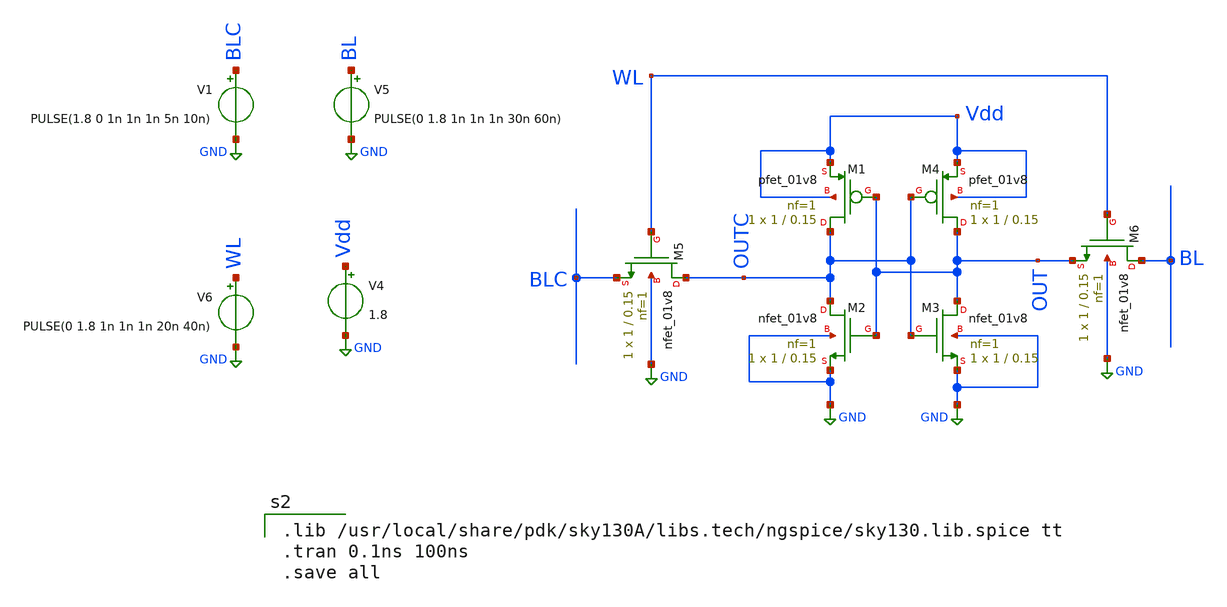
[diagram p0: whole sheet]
** sch_path: Schematic/SRam/SRam.sch
**.subckt SRam
XM2 OUTC OUT GND GND sky130_fd_pr__nfet_01v8 L=0.15 W=1 nf=1 ad='int((1 + 1)/2) * 1 / 1 * 0.29' as='int((1 + 2)/2) * 1 / 1 * 0.29'
+ pd='2*int((1 + 1)/2) * (1 / 1 + 0.29)' ps='2*int((1 + 2)/2) * (1 / 1 + 0.29)' nrd='0.29 / 1 ' nrs='0.29 / 1 '
+ sa=0 sb=0 sd=0 mult=1 m=1
XM1 OUTC OUT Vdd Vdd sky130_fd_pr__pfet_01v8 L=0.15 W=1 nf=1 ad='int((1 + 1)/2) * 1 / 1 * 0.29' as='int((1 + 2)/2) * 1 / 1 * 0.29'
+ pd='2*int((1 + 1)/2) * (1 / 1 + 0.29)' ps='2*int((1 + 2)/2) * (1 / 1 + 0.29)' nrd='0.29 / 1 ' nrs='0.29 / 1 '
+ sa=0 sb=0 sd=0 mult=1 m=1
XM3 OUT OUTC GND GND sky130_fd_pr__nfet_01v8 L=0.15 W=1 nf=1 ad='int((1 + 1)/2) * 1 / 1 * 0.29' as='int((1 + 2)/2) * 1 / 1 * 0.29'
+ pd='2*int((1 + 1)/2) * (1 / 1 + 0.29)' ps='2*int((1 + 2)/2) * (1 / 1 + 0.29)' nrd='0.29 / 1 ' nrs='0.29 / 1 '
+ sa=0 sb=0 sd=0 mult=1 m=1
XM4 OUT OUTC Vdd Vdd sky130_fd_pr__pfet_01v8 L=0.15 W=1 nf=1 ad='int((1 + 1)/2) * 1 / 1 * 0.29' as='int((1 + 2)/2) * 1 / 1 * 0.29'
+ pd='2*int((1 + 1)/2) * (1 / 1 + 0.29)' ps='2*int((1 + 2)/2) * (1 / 1 + 0.29)' nrd='0.29 / 1 ' nrs='0.29 / 1 '
+ sa=0 sb=0 sd=0 mult=1 m=1
XM5 OUTC WL BLC GND sky130_fd_pr__nfet_01v8 L=0.15 W=1 nf=1 ad='int((1 + 1)/2) * 1 / 1 * 0.29' as='int((1 + 2)/2) * 1 / 1 * 0.29'
+ pd='2*int((1 + 1)/2) * (1 / 1 + 0.29)' ps='2*int((1 + 2)/2) * (1 / 1 + 0.29)' nrd='0.29 / 1 ' nrs='0.29 / 1 '
+ sa=0 sb=0 sd=0 mult=1 m=1
XM6 BL WL OUT GND sky130_fd_pr__nfet_01v8 L=0.15 W=1 nf=1 ad='int((1 + 1)/2) * 1 / 1 * 0.29' as='int((1 + 2)/2) * 1 / 1 * 0.29'
+ pd='2*int((1 + 1)/2) * (1 / 1 + 0.29)' ps='2*int((1 + 2)/2) * (1 / 1 + 0.29)' nrd='0.29 / 1 ' nrs='0.29 / 1 '
+ sa=0 sb=0 sd=0 mult=1 m=1
V1 BLC GND PULSE(1.8 0 1n 1n 1n 5n 10n)
V4 Vdd GND 1.8
V5 BL GND PULSE(0 1.8 1n 1n 1n 30n 60n)
V6 WL GND PULSE(0 1.8 1n 1n 1n 20n 40n)
**** begin user architecture code

.lib /usr/local/share/pdk/sky130A/libs.tech/ngspice/sky130.lib.spice tt
.tran 0.1ns 100ns
.save all





**** end user architecture code
**.ends
.GLOBAL GND
.end
